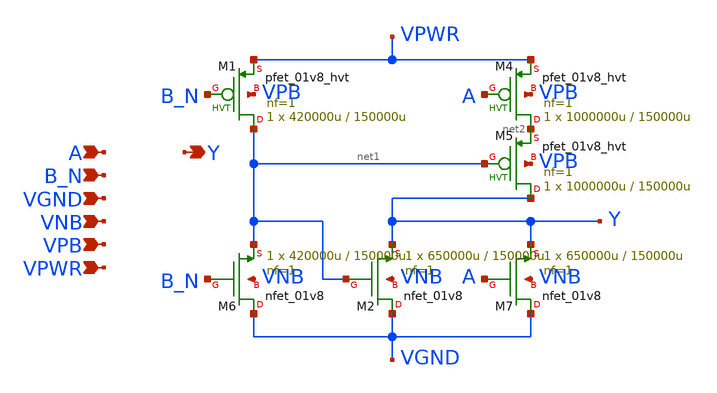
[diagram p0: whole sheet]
** sch_path: schematics/nor2b/sky130_fd_sc_hd__nor2b_1.sch
**.subckt sky130_fd_sc_hd__nor2b_1 A Y B_N VGND VNB VPB VPWR
*.ipin A
*.opin Y
*.ipin B_N
*.ipin VGND
*.ipin VNB
*.ipin VPB
*.ipin VPWR
XM1 net1 B_N VPWR VPB sky130_fd_pr__pfet_01v8_hvt L=150000u W=420000u nf=1 ad='int((1 + 1)/2) * 420000u / 1 * 0.29'
+ as='int((1 + 2)/2) * 420000u / 1 * 0.29' pd='2*int((1 + 1)/2) * (420000u / 1 + 0.29)' ps='2*int((1 + 2)/2) * (420000u / 1 + 0.29)'
+ nrd='0.29 / 420000u ' nrs='0.29 / 420000u ' sa=0 sb=0 sd=0 mult=1 m=1
XM2 VGND net1 Y VNB sky130_fd_pr__nfet_01v8 L=150000u W=650000u nf=1 ad='int((1 + 1)/2) * 650000u / 1 * 0.29'
+ as='int((1 + 2)/2) * 650000u / 1 * 0.29' pd='2*int((1 + 1)/2) * (650000u / 1 + 0.29)' ps='2*int((1 + 2)/2) * (650000u / 1 + 0.29)'
+ nrd='0.29 / 650000u ' nrs='0.29 / 650000u ' sa=0 sb=0 sd=0 mult=1 m=1
XM4 net2 A VPWR VPB sky130_fd_pr__pfet_01v8_hvt L=150000u W=1000000u nf=1 ad='int((1 + 1)/2) * 1000000u / 1 * 0.29'
+ as='int((1 + 2)/2) * 1000000u / 1 * 0.29' pd='2*int((1 + 1)/2) * (1000000u / 1 + 0.29)' ps='2*int((1 + 2)/2) * (1000000u / 1 + 0.29)'
+ nrd='0.29 / 1000000u ' nrs='0.29 / 1000000u ' sa=0 sb=0 sd=0 mult=1 m=1
XM5 Y net1 net2 VPB sky130_fd_pr__pfet_01v8_hvt L=150000u W=1000000u nf=1 ad='int((1 + 1)/2) * 1000000u / 1 * 0.29'
+ as='int((1 + 2)/2) * 1000000u / 1 * 0.29' pd='2*int((1 + 1)/2) * (1000000u / 1 + 0.29)' ps='2*int((1 + 2)/2) * (1000000u / 1 + 0.29)'
+ nrd='0.29 / 1000000u ' nrs='0.29 / 1000000u ' sa=0 sb=0 sd=0 mult=1 m=1
XM6 VGND B_N net1 VNB sky130_fd_pr__nfet_01v8 L=150000u W=420000u nf=1 ad='int((1 + 1)/2) * 420000u / 1 * 0.29'
+ as='int((1 + 2)/2) * 420000u / 1 * 0.29' pd='2*int((1 + 1)/2) * (420000u / 1 + 0.29)' ps='2*int((1 + 2)/2) * (420000u / 1 + 0.29)'
+ nrd='0.29 / 420000u ' nrs='0.29 / 420000u ' sa=0 sb=0 sd=0 mult=1 m=1
XM7 VGND A Y VNB sky130_fd_pr__nfet_01v8 L=150000u W=650000u nf=1 ad='int((1 + 1)/2) * 650000u / 1 * 0.29'
+ as='int((1 + 2)/2) * 650000u / 1 * 0.29' pd='2*int((1 + 1)/2) * (650000u / 1 + 0.29)' ps='2*int((1 + 2)/2) * (650000u / 1 + 0.29)'
+ nrd='0.29 / 650000u ' nrs='0.29 / 650000u ' sa=0 sb=0 sd=0 mult=1 m=1
**.ends
.end
